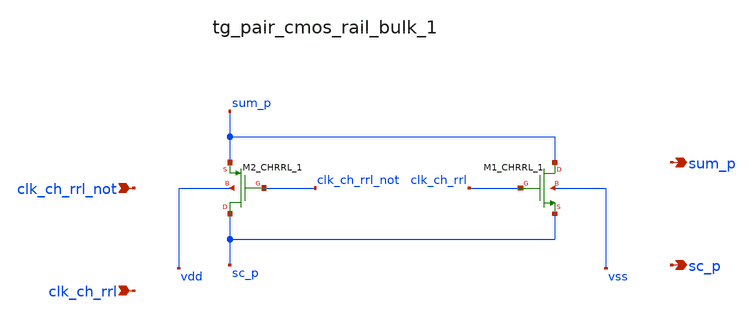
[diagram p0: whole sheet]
** sch_path: analog-db/raw/sup_003_rrl_sc_integrator/hier/blocks/tg_pair_cmos_rail_bulk_1.sch
**.subckt tg_pair_cmos_rail_bulk_1 clk_ch_rrl_not clk_ch_rrl sum_p sc_p
*.ipin clk_ch_rrl_not
*.ipin clk_ch_rrl
*.opin sum_p
*.opin sc_p
XM1_CHRRL_1 sum_p clk_ch_rrl sc_p vss sg13_lv_nmos w=x_dut_xm1_chrrl_1_w l=x_dut_xm1_chrrl_1_l ng=1
+ m=x_dut_xm1_chrrl_1_m
XM2_CHRRL_1 sc_p clk_ch_rrl_not sum_p vdd sg13_lv_pmos w=x_dut_xm2_chrrl_1_w l=x_dut_xm2_chrrl_1_l
+ ng=1 m=x_dut_xm2_chrrl_1_m
**.ends
.end
